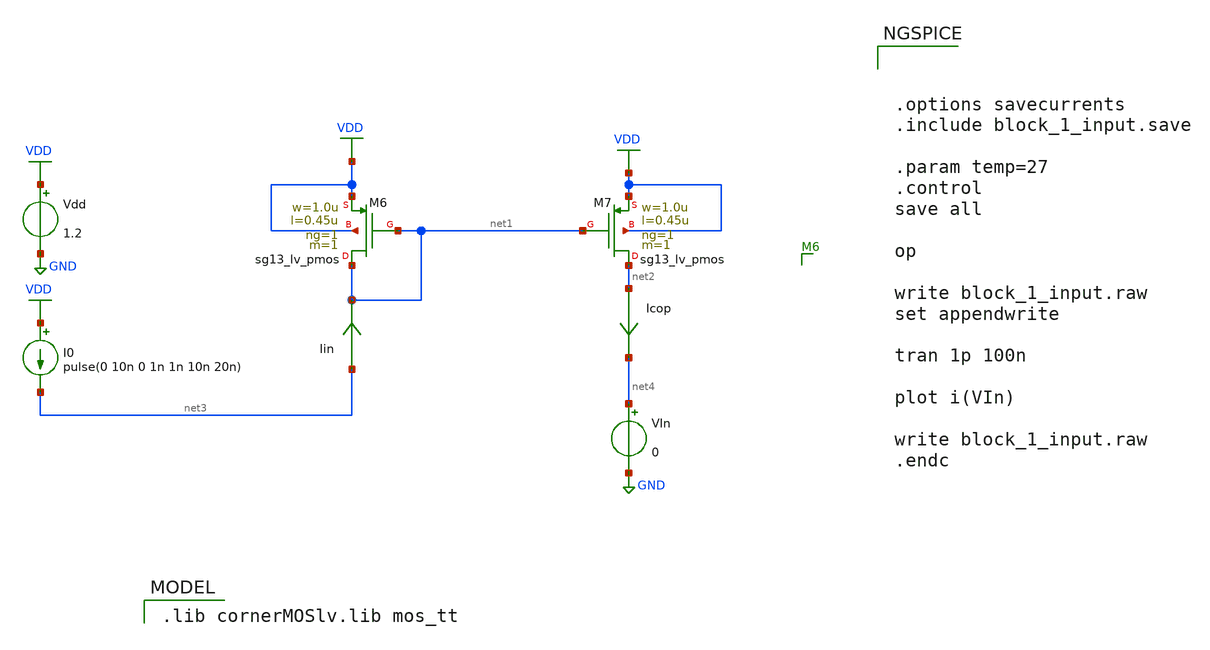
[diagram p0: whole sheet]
** sch_path: blocks/composite/dpi_adexp_neuron/design_data/xschem/legacy/block_1_input.sch
* Copyright 2023 IHP PDK Authors
**.subckt block_1_input
XM6 net1 net1 VDD VDD sg13_lv_pmos w=1.0u l=0.45u ng=1 m=1 mm_ok=1
XM7 net2 net1 VDD VDD sg13_lv_pmos w=1.0u l=0.45u ng=1 m=1 mm_ok=1
Icop net2 net4 0
.save i(icop)
Vdd VDD GND 1.2
I0 VDD net3 pulse(0 10n 0 1n 1n 10n 20n)
Iin net3 net1 0
.save i(iin)
VIn net4 GND 0
**** begin user architecture code



.options savecurrents
.include block_1_input.save

.param temp=27
.control
save all

op

write block_1_input.raw
set appendwrite

tran 1p 100n

plot i(VIn)

write block_1_input.raw
.endc


 .lib cornerMOSlv.lib mos_tt

**** end user architecture code
**.ends
.GLOBAL VDD
.GLOBAL GND
.end
